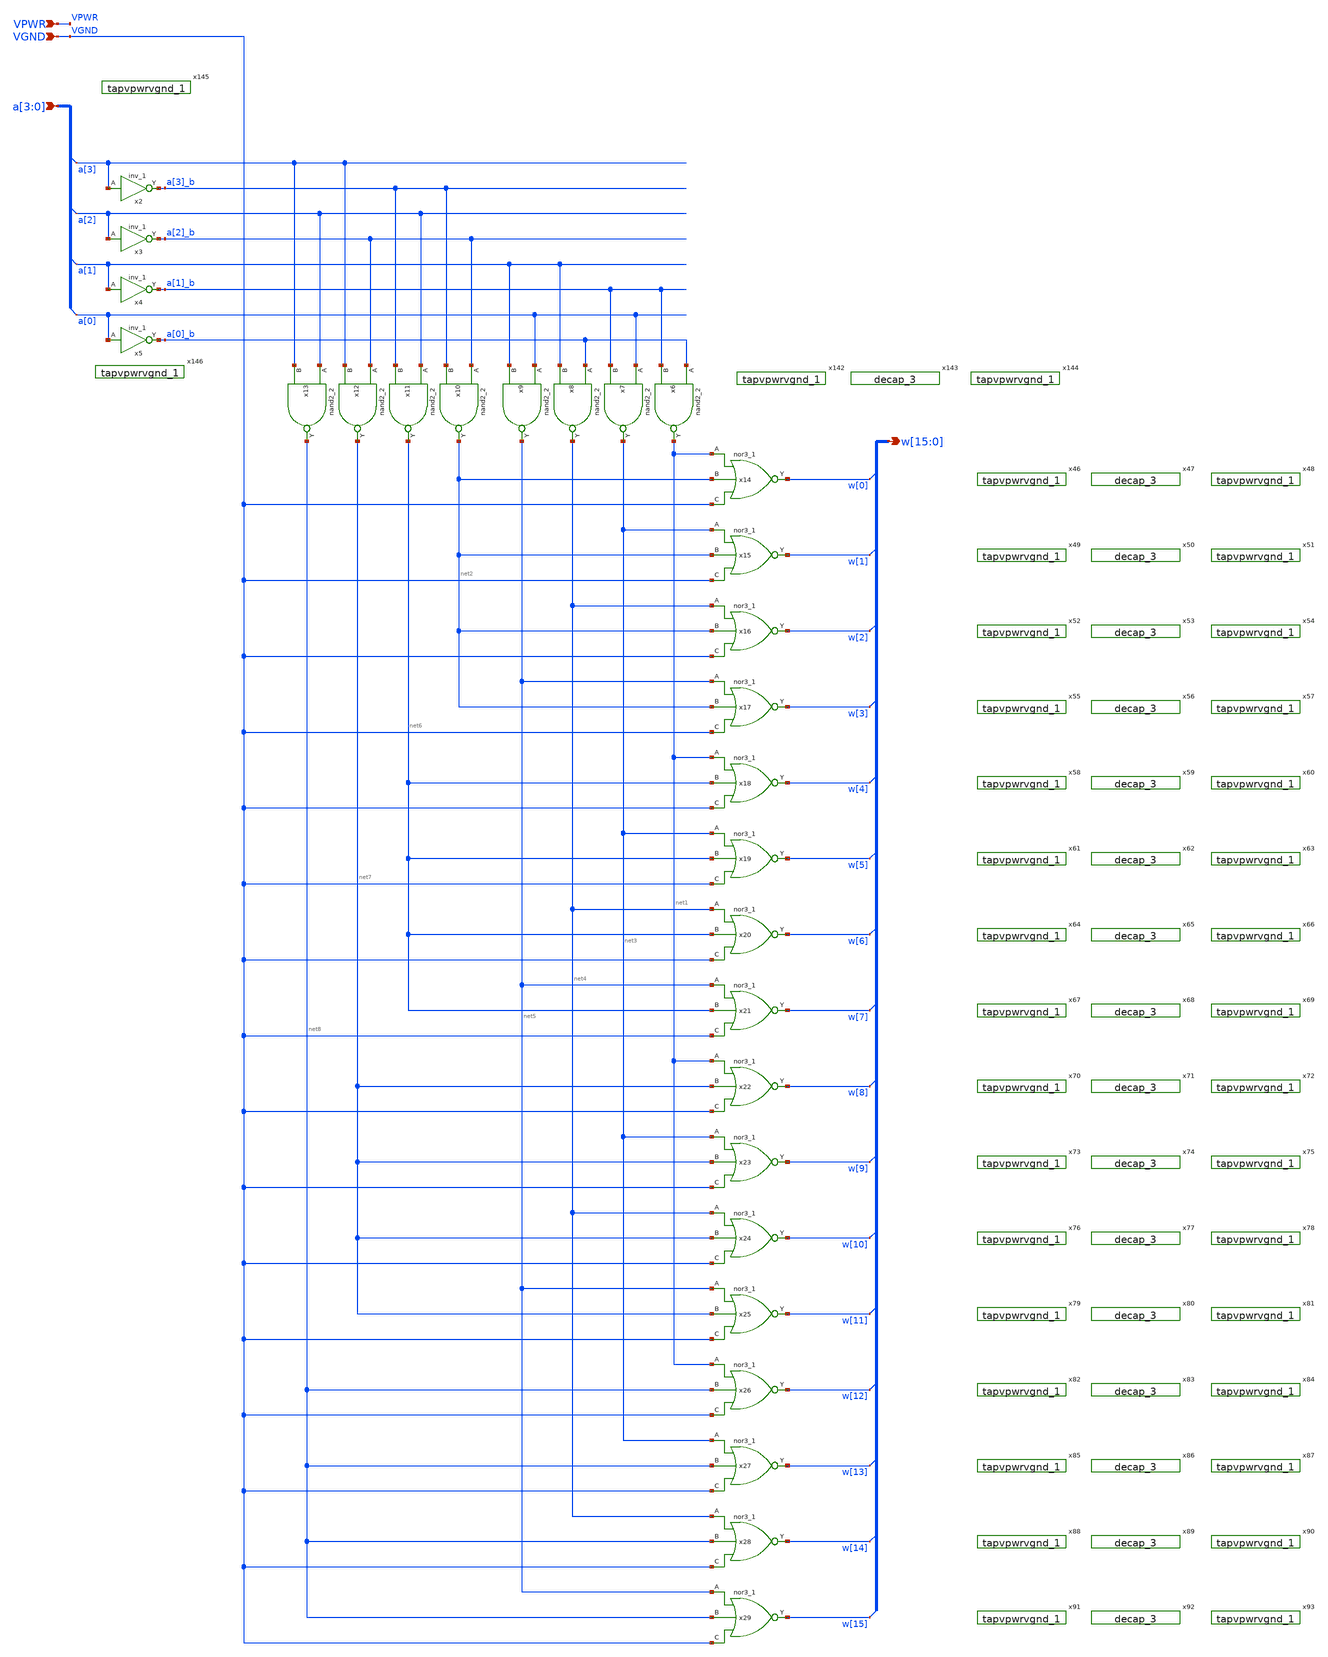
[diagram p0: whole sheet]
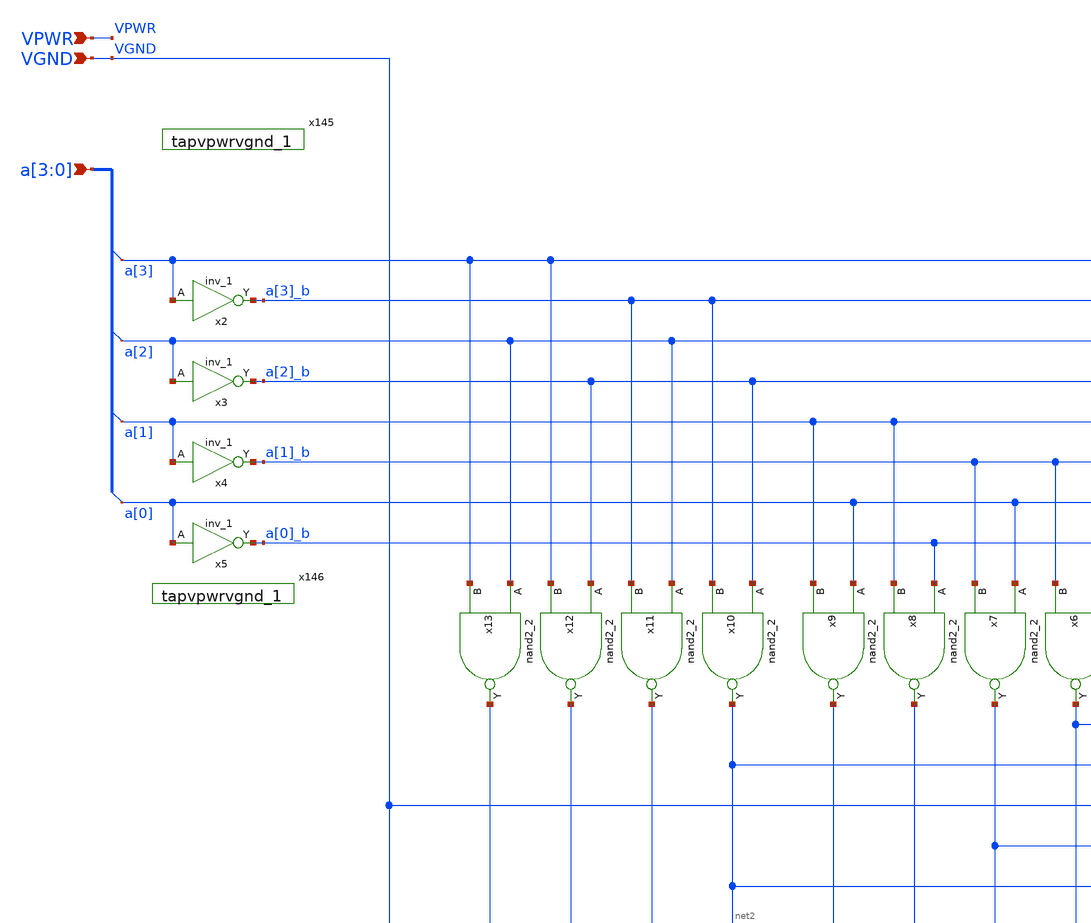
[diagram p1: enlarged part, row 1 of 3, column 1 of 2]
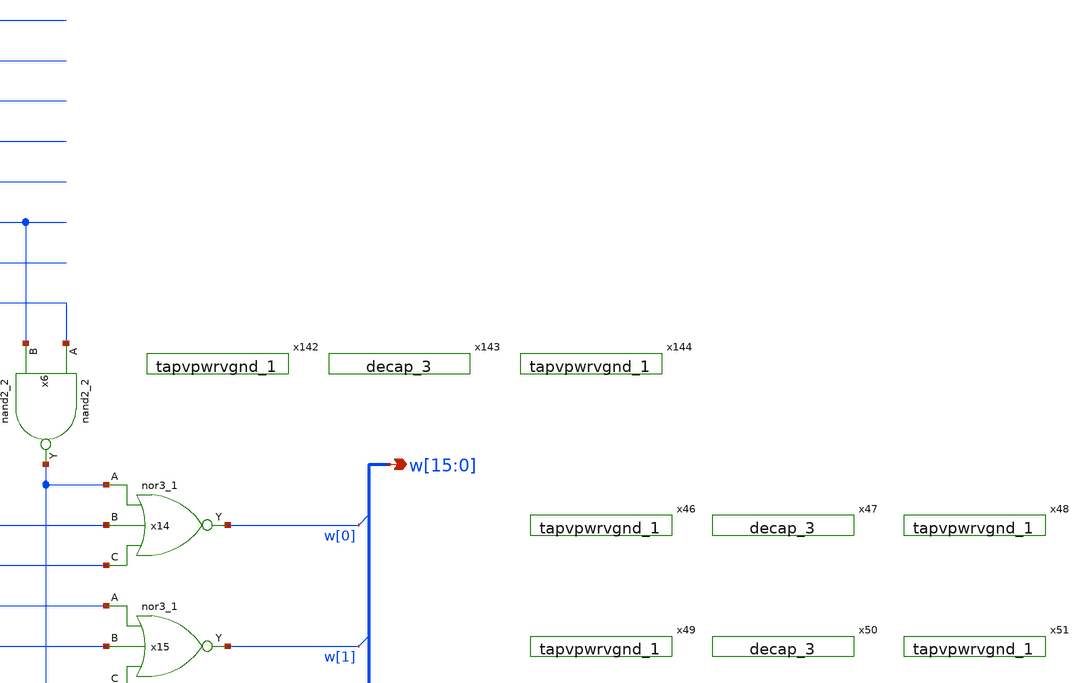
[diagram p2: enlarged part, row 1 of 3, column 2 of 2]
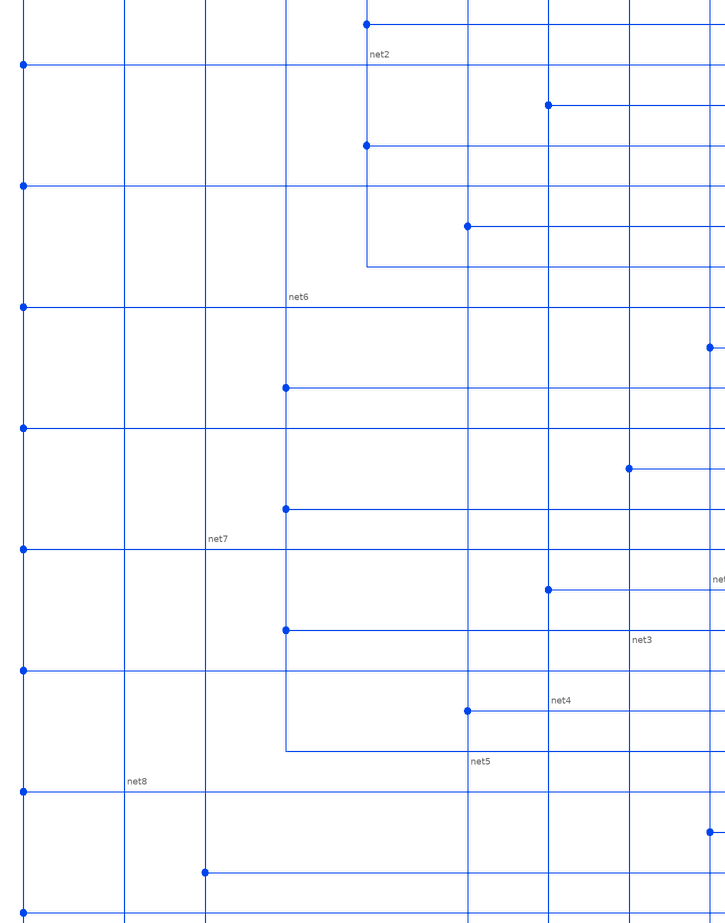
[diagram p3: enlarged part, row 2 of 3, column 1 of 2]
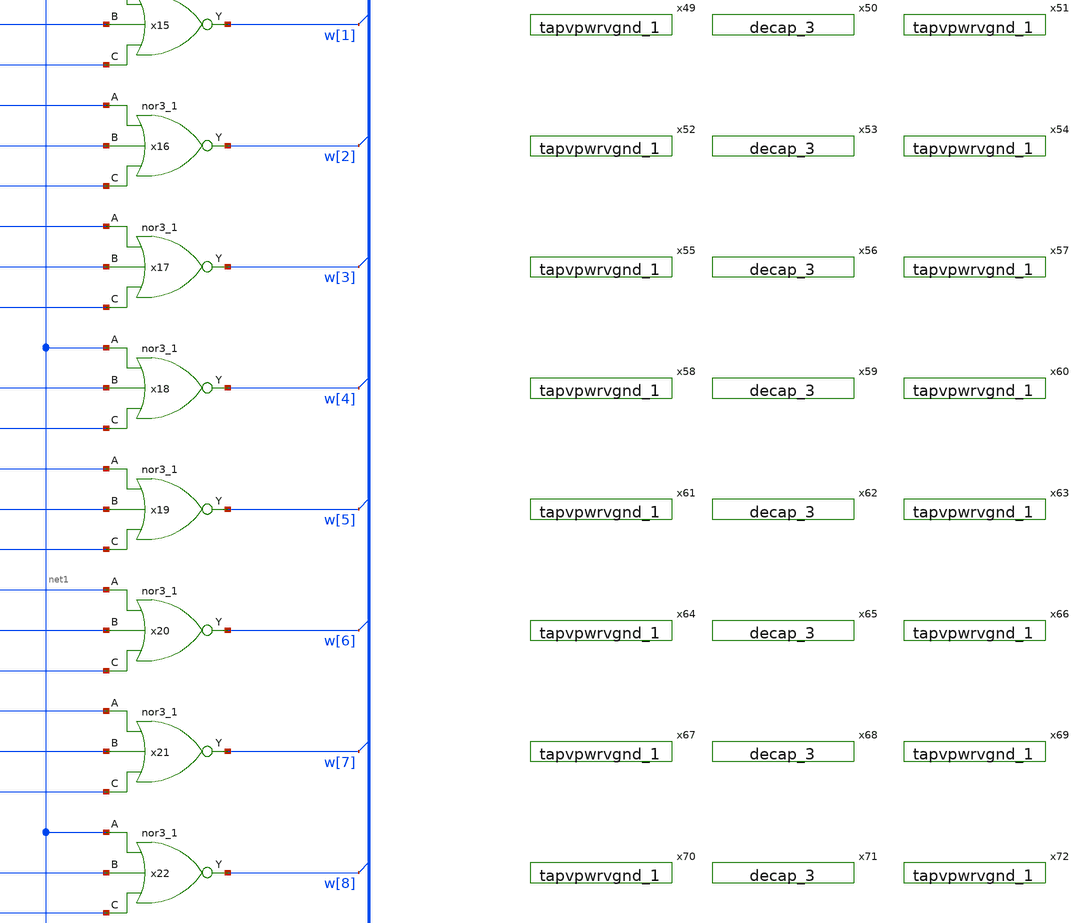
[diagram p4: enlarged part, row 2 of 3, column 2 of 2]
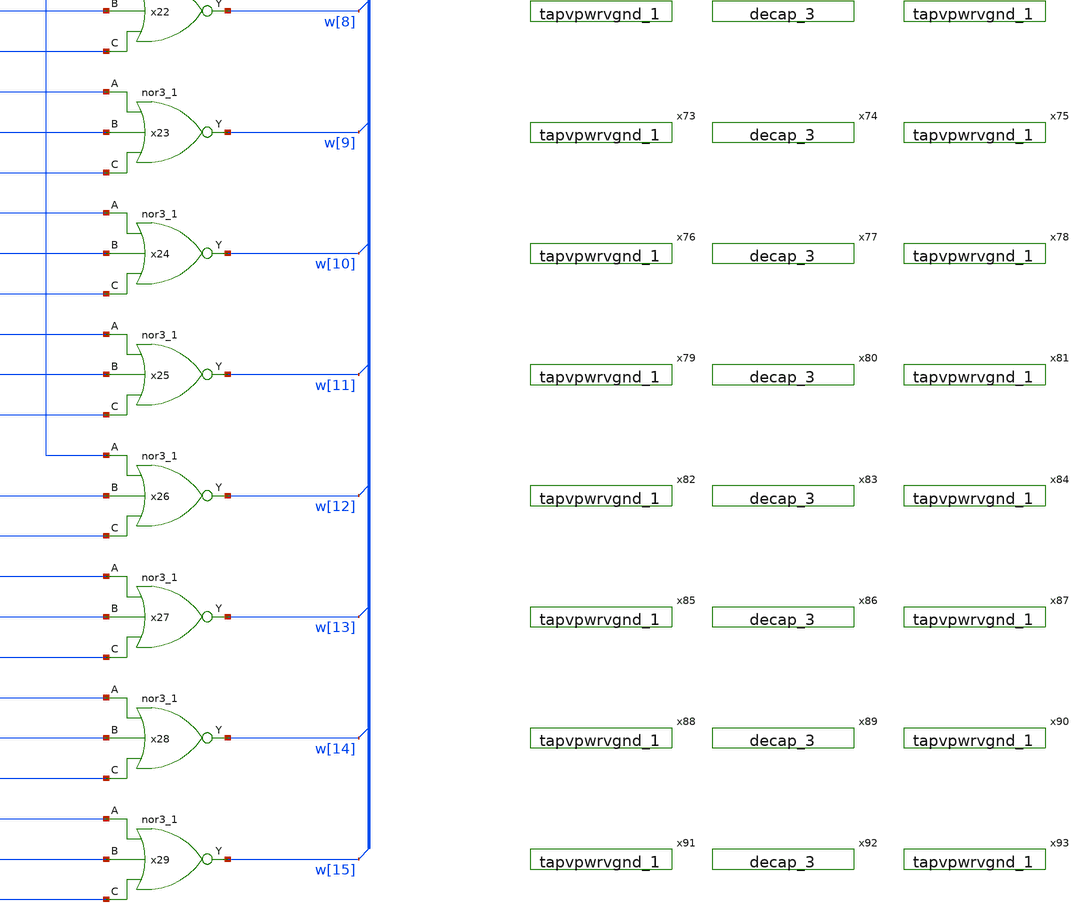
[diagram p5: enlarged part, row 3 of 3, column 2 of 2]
** sch_path: xschem/array_column_decode.sch
**.subckt array_column_decode a[3],a[2],a[1],a[0] VPWR VGND
*+ w[15],w[14],w[13],w[12],w[11],w[10],w[9],w[8],w[7],w[6],w[5],w[4],w[3],w[2],w[1],w[0]
*.ipin a[3],a[2],a[1],a[0]
*.ipin VPWR
*.ipin VGND
*.opin w[15],w[14],w[13],w[12],w[11],w[10],w[9],w[8],w[7],w[6],w[5],w[4],w[3],w[2],w[1],w[0]
x2 a[3] VGND VGND VPWR VPWR a[3]_b sky130_fd_sc_hd__inv_1
x3 a[2] VGND VGND VPWR VPWR a[2]_b sky130_fd_sc_hd__inv_1
x4 a[1] VGND VGND VPWR VPWR a[1]_b sky130_fd_sc_hd__inv_1
x5 a[0] VGND VGND VPWR VPWR a[0]_b sky130_fd_sc_hd__inv_1
x13 a[2] a[3] VGND VGND VPWR VPWR net8 sky130_fd_sc_hd__nand2_2
x6 a[0]_b a[1]_b VGND VGND VPWR VPWR net1 sky130_fd_sc_hd__nand2_2
x7 a[0] a[1]_b VGND VGND VPWR VPWR net3 sky130_fd_sc_hd__nand2_2
x8 a[0]_b a[1] VGND VGND VPWR VPWR net4 sky130_fd_sc_hd__nand2_2
x9 a[0] a[1] VGND VGND VPWR VPWR net5 sky130_fd_sc_hd__nand2_2
x10 a[2]_b a[3]_b VGND VGND VPWR VPWR net2 sky130_fd_sc_hd__nand2_2
x11 a[2] a[3]_b VGND VGND VPWR VPWR net6 sky130_fd_sc_hd__nand2_2
x12 a[2]_b a[3] VGND VGND VPWR VPWR net7 sky130_fd_sc_hd__nand2_2
x14 net1 net2 VGND VGND VGND VPWR VPWR w[0] sky130_fd_sc_hd__nor3_1
x15 net3 net2 VGND VGND VGND VPWR VPWR w[1] sky130_fd_sc_hd__nor3_1
x16 net4 net2 VGND VGND VGND VPWR VPWR w[2] sky130_fd_sc_hd__nor3_1
x17 net5 net2 VGND VGND VGND VPWR VPWR w[3] sky130_fd_sc_hd__nor3_1
x18 net1 net6 VGND VGND VGND VPWR VPWR w[4] sky130_fd_sc_hd__nor3_1
x19 net3 net6 VGND VGND VGND VPWR VPWR w[5] sky130_fd_sc_hd__nor3_1
x20 net4 net6 VGND VGND VGND VPWR VPWR w[6] sky130_fd_sc_hd__nor3_1
x21 net5 net6 VGND VGND VGND VPWR VPWR w[7] sky130_fd_sc_hd__nor3_1
x22 net1 net7 VGND VGND VGND VPWR VPWR w[8] sky130_fd_sc_hd__nor3_1
x23 net3 net7 VGND VGND VGND VPWR VPWR w[9] sky130_fd_sc_hd__nor3_1
x24 net4 net7 VGND VGND VGND VPWR VPWR w[10] sky130_fd_sc_hd__nor3_1
x25 net5 net7 VGND VGND VGND VPWR VPWR w[11] sky130_fd_sc_hd__nor3_1
x26 net1 net8 VGND VGND VGND VPWR VPWR w[12] sky130_fd_sc_hd__nor3_1
x27 net3 net8 VGND VGND VGND VPWR VPWR w[13] sky130_fd_sc_hd__nor3_1
x28 net4 net8 VGND VGND VGND VPWR VPWR w[14] sky130_fd_sc_hd__nor3_1
x29 net5 net8 VGND VGND VGND VPWR VPWR w[15] sky130_fd_sc_hd__nor3_1
x46 VGND VPWR sky130_fd_sc_hd__tapvpwrvgnd_1
x47 VGND VGND VPWR VPWR sky130_fd_sc_hd__decap_3
x48 VGND VPWR sky130_fd_sc_hd__tapvpwrvgnd_1
x49 VGND VPWR sky130_fd_sc_hd__tapvpwrvgnd_1
x50 VGND VGND VPWR VPWR sky130_fd_sc_hd__decap_3
x51 VGND VPWR sky130_fd_sc_hd__tapvpwrvgnd_1
x52 VGND VPWR sky130_fd_sc_hd__tapvpwrvgnd_1
x53 VGND VGND VPWR VPWR sky130_fd_sc_hd__decap_3
x54 VGND VPWR sky130_fd_sc_hd__tapvpwrvgnd_1
x55 VGND VPWR sky130_fd_sc_hd__tapvpwrvgnd_1
x56 VGND VGND VPWR VPWR sky130_fd_sc_hd__decap_3
x57 VGND VPWR sky130_fd_sc_hd__tapvpwrvgnd_1
x58 VGND VPWR sky130_fd_sc_hd__tapvpwrvgnd_1
x59 VGND VGND VPWR VPWR sky130_fd_sc_hd__decap_3
x60 VGND VPWR sky130_fd_sc_hd__tapvpwrvgnd_1
x61 VGND VPWR sky130_fd_sc_hd__tapvpwrvgnd_1
x62 VGND VGND VPWR VPWR sky130_fd_sc_hd__decap_3
x63 VGND VPWR sky130_fd_sc_hd__tapvpwrvgnd_1
x64 VGND VPWR sky130_fd_sc_hd__tapvpwrvgnd_1
x65 VGND VGND VPWR VPWR sky130_fd_sc_hd__decap_3
x66 VGND VPWR sky130_fd_sc_hd__tapvpwrvgnd_1
x67 VGND VPWR sky130_fd_sc_hd__tapvpwrvgnd_1
x68 VGND VGND VPWR VPWR sky130_fd_sc_hd__decap_3
x69 VGND VPWR sky130_fd_sc_hd__tapvpwrvgnd_1
x70 VGND VPWR sky130_fd_sc_hd__tapvpwrvgnd_1
x71 VGND VGND VPWR VPWR sky130_fd_sc_hd__decap_3
x72 VGND VPWR sky130_fd_sc_hd__tapvpwrvgnd_1
x73 VGND VPWR sky130_fd_sc_hd__tapvpwrvgnd_1
x74 VGND VGND VPWR VPWR sky130_fd_sc_hd__decap_3
x75 VGND VPWR sky130_fd_sc_hd__tapvpwrvgnd_1
x76 VGND VPWR sky130_fd_sc_hd__tapvpwrvgnd_1
x77 VGND VGND VPWR VPWR sky130_fd_sc_hd__decap_3
x78 VGND VPWR sky130_fd_sc_hd__tapvpwrvgnd_1
x79 VGND VPWR sky130_fd_sc_hd__tapvpwrvgnd_1
x80 VGND VGND VPWR VPWR sky130_fd_sc_hd__decap_3
x81 VGND VPWR sky130_fd_sc_hd__tapvpwrvgnd_1
x82 VGND VPWR sky130_fd_sc_hd__tapvpwrvgnd_1
x83 VGND VGND VPWR VPWR sky130_fd_sc_hd__decap_3
x84 VGND VPWR sky130_fd_sc_hd__tapvpwrvgnd_1
x85 VGND VPWR sky130_fd_sc_hd__tapvpwrvgnd_1
x86 VGND VGND VPWR VPWR sky130_fd_sc_hd__decap_3
x87 VGND VPWR sky130_fd_sc_hd__tapvpwrvgnd_1
x88 VGND VPWR sky130_fd_sc_hd__tapvpwrvgnd_1
x89 VGND VGND VPWR VPWR sky130_fd_sc_hd__decap_3
x90 VGND VPWR sky130_fd_sc_hd__tapvpwrvgnd_1
x91 VGND VPWR sky130_fd_sc_hd__tapvpwrvgnd_1
x92 VGND VGND VPWR VPWR sky130_fd_sc_hd__decap_3
x93 VGND VPWR sky130_fd_sc_hd__tapvpwrvgnd_1
x142 VGND VPWR sky130_fd_sc_hd__tapvpwrvgnd_1
x143 VGND VGND VPWR VPWR sky130_fd_sc_hd__decap_3
x144 VGND VPWR sky130_fd_sc_hd__tapvpwrvgnd_1
x145 VGND VPWR sky130_fd_sc_hd__tapvpwrvgnd_1
x146 VGND VPWR sky130_fd_sc_hd__tapvpwrvgnd_1
**** begin user architecture code
 .lib $::SKYWATER_MODELS/sky130.lib.spice tt

.include $::SKYWATER_STDCELLS/sky130_fd_sc_hd.spice



**** end user architecture code
**.ends
.end
